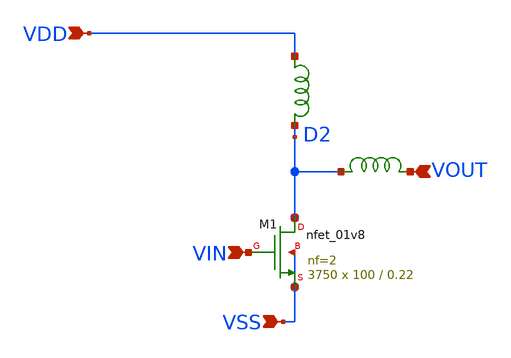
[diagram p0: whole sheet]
** sch_path: design/LELO_SVOD_SKY130A/LELO_AC.sch
**.subckt LELO_AC VDD VIN VOUT VSS
*.ipin VDD
*.ipin VIN
*.ipin VOUT
*.ipin VSS
XM1 D2 VIN VSS VSS sky130_fd_pr__nfet_01v8 L=0.22 W=100 nf=2 ad='int((nf+1)/2) * W/nf * 0.29' as='int((nf+2)/2) * W/nf * 0.29'
+ pd='2*int((nf+1)/2) * (W/nf + 0.29)' ps='2*int((nf+2)/2) * (W/nf + 0.29)' nrd='0.29 / W' nrs='0.29 / W'
+ sa=0 sb=0 sd=0 mult=3750 m=3750
x2 VDD D2 LQW2BAN3N2J00
x4 D2 VOUT LQW2BASR39J00
**.ends

* expanding   symbol:  LELO_SVOD_SKY130A/LQW2BAN3N2J00.sym # of pins=2
** sym_path: design/LELO_SVOD_SKY130A/LQW2BAN3N2J00.sym
.SUBCKT LQW2BAN3N2J00 port1 port2
C1 port1 port2 2.87e-14
L2 port1 1 2.96e-9
R2 1 port2 1.30e-2
R3 port1 port2 4.40e+3
L4 port1 2 2.67e-8
R4 2 port2 2.47
L5 port1 3 5.23e-8
R5 3 port2 20.8
L6 port1 4 1.23e-7
R6 4 port2 692
.ENDS LQW2BAN3N2J00

* expanding   symbol:  LELO_SVOD_SKY130A/LQW2BASR39J00.sym # of pins=2
** sym_path: design/LELO_SVOD_SKY130A/LQW2BASR39J00.sym
.SUBCKT LQW2BASR39J00 port1 port2
C1 port1 port2 7.29e-14
L2 port1 1 4.17e-7
R2 1 port2 1.32
R3 port1 port2 5.58e+4
L4 port1 2 1.18e-5
R4 2 port2 314
L5 port1 3 1.66e-5
R5 3 port2 4.79e+3
L6 port1 4 1.63e-4
R6 4 port2 2.88e+4
L7 port1 5 1.52e-6
C7 5 6 1.12e-14
R7 6 port2 1.12e+3
L8 port1 7 1.87e-5
C8 7 8 2.68e-16
R8 8 port2 1.14e+4
L9 port1 9 4.56e-6
C9 9 10 3.24e-16
R9 10 port2 4.95e+3
L10 port1 11 9.07e-7
C10 11 12 7.16e-16
R10 12 port2 1.93e+3
L11 port1 13 1.05e-6
C11 13 14 3.53e-16
R11 14 port2 2.19e+3
L12 port1 15 1.67e-7
C12 15 16 1.04e-15
R12 16 port2 603
.ENDS LQW2BASR39J00

.end
